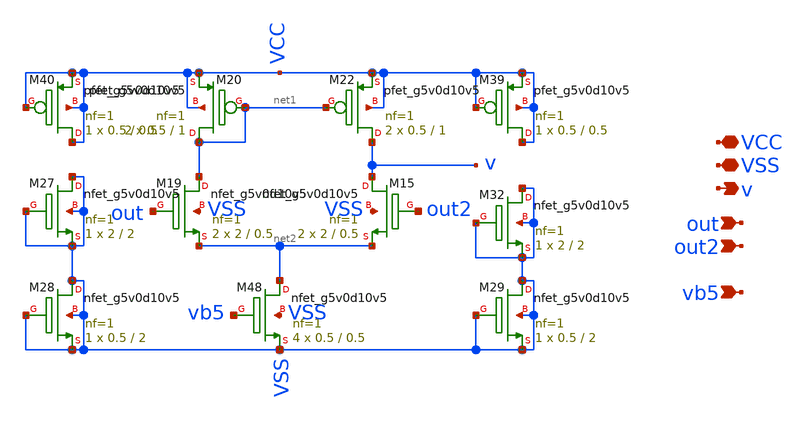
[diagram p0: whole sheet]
** sch_path: latest_working_comparator/single_ended.sch
**.subckt single_ended VCC VSS v out out2 vb5
*.iopin VCC
*.iopin VSS
*.opin v
*.ipin out
*.ipin out2
*.ipin vb5
XM20 net1 net1 VCC VCC sky130_fd_pr__pfet_g5v0d10v5 L=1 W=0.5 nf=1 ad='int((nf+1)/2) * W/nf * 0.29' as='int((nf+2)/2) * W/nf * 0.29'
+ pd='2*int((nf+1)/2) * (W/nf + 0.29)' ps='2*int((nf+2)/2) * (W/nf + 0.29)' nrd='0.29 / W' nrs='0.29 / W'
+ sa=0 sb=0 sd=0 mult=2 m=2
XM22 v net1 VCC VCC sky130_fd_pr__pfet_g5v0d10v5 L=1 W=0.5 nf=1 ad='int((nf+1)/2) * W/nf * 0.29' as='int((nf+2)/2) * W/nf * 0.29'
+ pd='2*int((nf+1)/2) * (W/nf + 0.29)' ps='2*int((nf+2)/2) * (W/nf + 0.29)' nrd='0.29 / W' nrs='0.29 / W'
+ sa=0 sb=0 sd=0 mult=2 m=2
XM15 v out2 net2 VSS sky130_fd_pr__nfet_g5v0d10v5 L=0.5 W=2 nf=1 ad='int((nf+1)/2) * W/nf * 0.29' as='int((nf+2)/2) * W/nf * 0.29'
+ pd='2*int((nf+1)/2) * (W/nf + 0.29)' ps='2*int((nf+2)/2) * (W/nf + 0.29)' nrd='0.29 / W' nrs='0.29 / W'
+ sa=0 sb=0 sd=0 mult=2 m=2
XM19 net1 out net2 VSS sky130_fd_pr__nfet_g5v0d10v5 L=0.5 W=2 nf=1 ad='int((nf+1)/2) * W/nf * 0.29' as='int((nf+2)/2) * W/nf * 0.29'
+ pd='2*int((nf+1)/2) * (W/nf + 0.29)' ps='2*int((nf+2)/2) * (W/nf + 0.29)' nrd='0.29 / W' nrs='0.29 / W'
+ sa=0 sb=0 sd=0 mult=2 m=2
XM48 net2 vb5 VSS VSS sky130_fd_pr__nfet_g5v0d10v5 L=0.5 W=0.5 nf=1 ad='int((nf+1)/2) * W/nf * 0.29'
+ as='int((nf+2)/2) * W/nf * 0.29' pd='2*int((nf+1)/2) * (W/nf + 0.29)' ps='2*int((nf+2)/2) * (W/nf + 0.29)'
+ nrd='0.29 / W' nrs='0.29 / W' sa=0 sb=0 sd=0 mult=4 m=4
XM27 VSS VSS VSS VSS sky130_fd_pr__nfet_g5v0d10v5 L=2 W=2 nf=1 ad='int((nf+1)/2) * W/nf * 0.29' as='int((nf+2)/2) * W/nf * 0.29'
+ pd='2*int((nf+1)/2) * (W/nf + 0.29)' ps='2*int((nf+2)/2) * (W/nf + 0.29)' nrd='0.29 / W' nrs='0.29 / W'
+ sa=0 sb=0 sd=0 mult=1 m=1
XM28 VSS VSS VSS VSS sky130_fd_pr__nfet_g5v0d10v5 L=2 W=0.5 nf=1 ad='int((nf+1)/2) * W/nf * 0.29' as='int((nf+2)/2) * W/nf * 0.29'
+ pd='2*int((nf+1)/2) * (W/nf + 0.29)' ps='2*int((nf+2)/2) * (W/nf + 0.29)' nrd='0.29 / W' nrs='0.29 / W'
+ sa=0 sb=0 sd=0 mult=1 m=1
XM29 VSS VSS VSS VSS sky130_fd_pr__nfet_g5v0d10v5 L=2 W=0.5 nf=1 ad='int((nf+1)/2) * W/nf * 0.29' as='int((nf+2)/2) * W/nf * 0.29'
+ pd='2*int((nf+1)/2) * (W/nf + 0.29)' ps='2*int((nf+2)/2) * (W/nf + 0.29)' nrd='0.29 / W' nrs='0.29 / W'
+ sa=0 sb=0 sd=0 mult=1 m=1
XM32 VSS VSS VSS VSS sky130_fd_pr__nfet_g5v0d10v5 L=2 W=2 nf=1 ad='int((nf+1)/2) * W/nf * 0.29' as='int((nf+2)/2) * W/nf * 0.29'
+ pd='2*int((nf+1)/2) * (W/nf + 0.29)' ps='2*int((nf+2)/2) * (W/nf + 0.29)' nrd='0.29 / W' nrs='0.29 / W'
+ sa=0 sb=0 sd=0 mult=1 m=1
XM39 VCC VCC VCC VCC sky130_fd_pr__pfet_g5v0d10v5 L=0.5 W=0.5 nf=1 ad='int((nf+1)/2) * W/nf * 0.29' as='int((nf+2)/2) * W/nf * 0.29'
+ pd='2*int((nf+1)/2) * (W/nf + 0.29)' ps='2*int((nf+2)/2) * (W/nf + 0.29)' nrd='0.29 / W' nrs='0.29 / W'
+ sa=0 sb=0 sd=0 mult=1 m=1
XM40 VCC VCC VCC VCC sky130_fd_pr__pfet_g5v0d10v5 L=0.5 W=0.5 nf=1 ad='int((nf+1)/2) * W/nf * 0.29' as='int((nf+2)/2) * W/nf * 0.29'
+ pd='2*int((nf+1)/2) * (W/nf + 0.29)' ps='2*int((nf+2)/2) * (W/nf + 0.29)' nrd='0.29 / W' nrs='0.29 / W'
+ sa=0 sb=0 sd=0 mult=1 m=1
**.ends
.end
